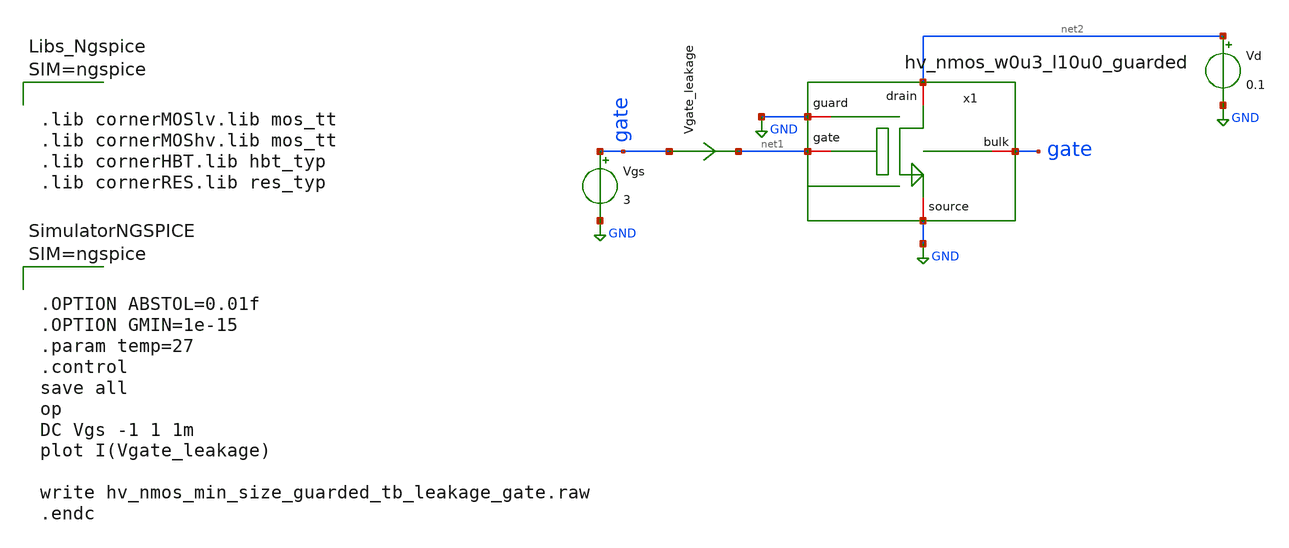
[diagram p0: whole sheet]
** sch_path: trident_test_structures/design_data/xschem/transistor_characterization/hv_nmos_w0u3_l10u0_guarded/hv_nmos_w0u3_l10u0_guarded_tb_leakage_gate.sch
**.subckt hv_nmos_w0u3_l10u0_guarded_tb_leakage_gate
Vgs gate GND 3
Vgate_leakage gate net1 0
.save i(vgate_leakage)
Vd net2 GND 0.1
x1 net2 GND net1 gate GND hv_nmos_w0u3_l10u0_guarded
**** begin user architecture code



.lib cornerMOSlv.lib mos_tt
.lib cornerMOShv.lib mos_tt
.lib cornerHBT.lib hbt_typ
.lib cornerRES.lib res_typ






.OPTION ABSTOL=0.01f
.OPTION GMIN=1e-15
.param temp=27
.control
save all
op
DC Vgs -1 1 1m
plot I(Vgate_leakage)

write hv_nmos_min_size_guarded_tb_leakage_gate.raw
.endc



**** end user architecture code
**.ends

* expanding   symbol:  hv_nmos_w0u3_l10u0_guarded.sym # of pins=5
** sym_path: trident_test_structures/design_data/xschem/transistor_characterization/hv_nmos_w0u3_l10u0_guarded/hv_nmos_w0u3_l10u0_guarded.sym
** sch_path: trident_test_structures/design_data/xschem/transistor_characterization/hv_nmos_w0u3_l10u0_guarded/hv_nmos_w0u3_l10u0_guarded.sch
.subckt hv_nmos_w0u3_l10u0_guarded drain guard gate bulk source
*.iopin gate
*.iopin drain
*.iopin source
*.iopin bulk
*.iopin guard
XM1 drain gate source sub! sg13_hv_nmos w=0.3u l=10u ng=1 m=1 mm_ok=1
XR1 bulk sub! ptap1 R=32.37 w=10.33e-6 l=0.78e-6
.ends

.GLOBAL GND
.GLOBAL sub!
.end
